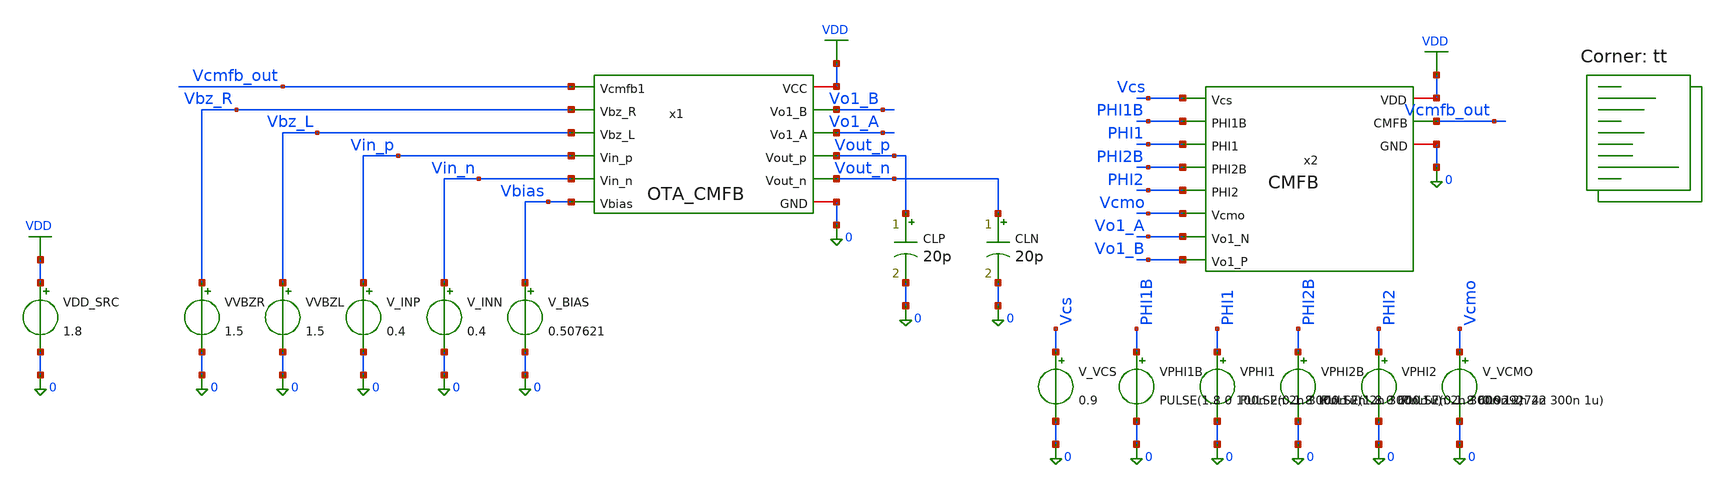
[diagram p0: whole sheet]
** sch_path: blocks/02_CMFB/sim/tb_OTA_CMFB_firststage_closedloop.sch
**.subckt tb_OTA_CMFB_firststage_closedloop
x1 VDD Vcmfb_out Vbz_R Vbz_L Vin_p Vin_n Vo1_B Vo1_A Vout_p Vout_n Vbias 0 OTA_CMFB
x2 Vcmfb_out Vcs PHI1B PHI1 VDD PHI2B 0 PHI2 Vcmo Vo1_A Vo1_B CMFB
VDD_SRC VDD 0 1.8
VVBZR Vbz_R 0 1.5
VVBZL Vbz_L 0 1.5
V_INP Vin_p 0 0.4
V_INN Vin_n 0 0.4
V_BIAS Vbias 0 0.507621
CLP Vout_p 0 20p m=1
CLN Vout_n 0 20p m=1
V_VCS Vcs 0 0.9
VPHI1B PHI1B 0 PULSE(1.8 0 100n 2n 2n 300n 1u)
VPHI1 PHI1 0 PULSE(0 1.8 100n 2n 2n 300n 1u)
VPHI2B PHI2B 0 PULSE(1.8 0 600n 2n 2n 300n 1u)
VPHI2 PHI2 0 PULSE(0 1.8 600n 2n 2n 300n 1u)
V_VCMO Vcmo 0 0.9292742
**** begin user architecture code
.lib $::SKYWATER_MODELS/sky130.lib.spice tt


* ==========================================================
* OTA + SC-CMFB CLOSED-LOOP VERIFICATION
* SKY130 TT | VDD = 1.8 V | TEMP = 27 C
*
* Simulation: 100 us
* Clock period: 1 us
* First-stage VCMO target: 0.9292742 V
*
* Closed-loop feedback:
* CMFB output = Vcmfb_out = OTA Vcmfb1 input
*
* No UIC
* ==========================================================

.options rshunt=1e12

RLEAK_CMFB Vcmfb_out 0 1e12

.control
save all

* ==========================================================
* 1. TRANSIENT SIMULATION
* ==========================================================

tran 1n 100u

* ==========================================================
* 2. COMMON-MODE AND DIFFERENTIAL VECTORS
* ==========================================================

let VO1CM_TRACE = (v(vo1_a)+v(vo1_b))/2
let VO1D_TRACE  = v(vo1_a)-v(vo1_b)

let VOCM_TRACE  = (v(vout_p)+v(vout_n))/2
let VOD_TRACE   = v(vout_p)-v(vout_n)

* ==========================================================
* 3. FIRST-STAGE STEADY STATE
* Measurement interval: 90-100 us
* ==========================================================

meas tran VO1A_AVG AVG v(vo1_a) FROM=90u TO=100u
meas tran VO1B_AVG AVG v(vo1_b) FROM=90u TO=100u

meas tran VO1CM_AVG AVG VO1CM_TRACE FROM=90u TO=100u
meas tran VO1CM_MIN MIN VO1CM_TRACE FROM=90u TO=100u
meas tran VO1CM_MAX MAX VO1CM_TRACE FROM=90u TO=100u

meas tran VO1D_AVG AVG VO1D_TRACE FROM=90u TO=100u

let VCMO_TARGET = 0.9292742

let VO1CM_ERROR = VO1CM_AVG-VCMO_TARGET
let VO1CM_ERROR_ABS = abs(VO1CM_ERROR)

let VO1CM_RIPPLE = VO1CM_MAX-VO1CM_MIN

* ==========================================================
* 4. FINAL OTA OUTPUT
* ==========================================================

meas tran VOUTP_AVG AVG v(vout_p) FROM=90u TO=100u
meas tran VOUTN_AVG AVG v(vout_n) FROM=90u TO=100u

meas tran VOCM_AVG AVG VOCM_TRACE FROM=90u TO=100u
meas tran VOCM_MIN MIN VOCM_TRACE FROM=90u TO=100u
meas tran VOCM_MAX MAX VOCM_TRACE FROM=90u TO=100u

meas tran VOD_AVG AVG VOD_TRACE FROM=90u TO=100u

let VOCM_RIPPLE = VOCM_MAX-VOCM_MIN

* ==========================================================
* 5. CLOSED-LOOP CMFB CONTROL
* Actual feedback node: Vcmfb_out
* ==========================================================

meas tran VCMFB_AVG AVG v(vcmfb_out) FROM=90u TO=100u
meas tran VCMFB_MIN MIN v(vcmfb_out) FROM=90u TO=100u
meas tran VCMFB_MAX MAX v(vcmfb_out) FROM=90u TO=100u

let VCMFB_RIPPLE = VCMFB_MAX-VCMFB_MIN

let VCMFB_NOMINAL = 0.9
let VCMFB_OFFSET = VCMFB_AVG-VCMFB_NOMINAL

* ==========================================================
* 6. LONG-TERM SETTLING CHECK
*
* Compare two consecutive 10-us windows
* ==========================================================

meas tran VO1CM_80_90 AVG VO1CM_TRACE FROM=80u TO=90u
meas tran VO1CM_90_100 AVG VO1CM_TRACE FROM=90u TO=100u

meas tran VCMFB_80_90 AVG v(vcmfb_out) FROM=80u TO=90u
meas tran VCMFB_90_100 AVG v(vcmfb_out) FROM=90u TO=100u

meas tran VOCM_80_90 AVG VOCM_TRACE FROM=80u TO=90u
meas tran VOCM_90_100 AVG VOCM_TRACE FROM=90u TO=100u

let CM_DRIFT = VO1CM_90_100-VO1CM_80_90
let CTRL_DRIFT = VCMFB_90_100-VCMFB_80_90
let OUT_DRIFT = VOCM_90_100-VOCM_80_90

let CM_DRIFT_ABS = abs(CM_DRIFT)
let CTRL_DRIFT_ABS = abs(CTRL_DRIFT)
let OUT_DRIFT_ABS = abs(OUT_DRIFT)

* ==========================================================
* 7. CLOCK VALIDATION
* ==========================================================

meas tran PHI1_MAX MAX v(phi1)
meas tran PHI1_MIN MIN v(phi1)

meas tran PHI1B_MAX MAX v(phi1b)
meas tran PHI1B_MIN MIN v(phi1b)

meas tran PHI2_MAX MAX v(phi2)
meas tran PHI2_MIN MIN v(phi2)

meas tran PHI2B_MAX MAX v(phi2b)
meas tran PHI2B_MIN MIN v(phi2b)

* ==========================================================
* 8. FIRST-STAGE RESULTS
* ==========================================================

echo ============================================
echo FIRST-STAGE CLOSED-LOOP RESULTS
echo ============================================

print VO1A_AVG
print VO1B_AVG

print VO1CM_AVG
print VO1CM_MIN
print VO1CM_MAX
print VO1CM_RIPPLE

print VO1D_AVG

print VCMO_TARGET
print VO1CM_ERROR
print VO1CM_ERROR_ABS

* ==========================================================
* 9. FINAL OUTPUT RESULTS
* ==========================================================

echo ============================================
echo FINAL OTA OUTPUT RESULTS
echo ============================================

print VOUTP_AVG
print VOUTN_AVG

print VOCM_AVG
print VOCM_MIN
print VOCM_MAX
print VOCM_RIPPLE

print VOD_AVG

* ==========================================================
* 10. CMFB CONTROL RESULTS
* ==========================================================

echo ============================================
echo CLOSED-LOOP CMFB RESULTS
echo ============================================

print VCMFB_AVG
print VCMFB_MIN
print VCMFB_MAX
print VCMFB_RIPPLE

print VCMFB_NOMINAL
print VCMFB_OFFSET

* ==========================================================
* 11. SETTLING AND LONG-TERM DRIFT
* ==========================================================

echo ============================================
echo LONG-TERM SETTLING RESULTS
echo ============================================

print VO1CM_80_90
print VO1CM_90_100

print VCMFB_80_90
print VCMFB_90_100

print VOCM_80_90
print VOCM_90_100

print CM_DRIFT
print CTRL_DRIFT
print OUT_DRIFT

print CM_DRIFT_ABS
print CTRL_DRIFT_ABS
print OUT_DRIFT_ABS

* ==========================================================
* 12. CLOCK RESULTS
* ==========================================================

echo ============================================
echo CLOCK VALIDATION
echo ============================================

print PHI1_MAX
print PHI1_MIN

print PHI1B_MAX
print PHI1B_MIN

print PHI2_MAX
print PHI2_MIN

print PHI2B_MAX
print PHI2B_MIN

* ==========================================================
* 13. WAVEFORMS
* ==========================================================

plot VO1CM_TRACE
plot v(vcmfb_out)

plot VOCM_TRACE

plot v(vo1_a) v(vo1_b)
plot v(vout_p) v(vout_n)

plot v(phi1) v(phi2)

.endc


**** end user architecture code
**.ends
.GLOBAL VDD
.end
